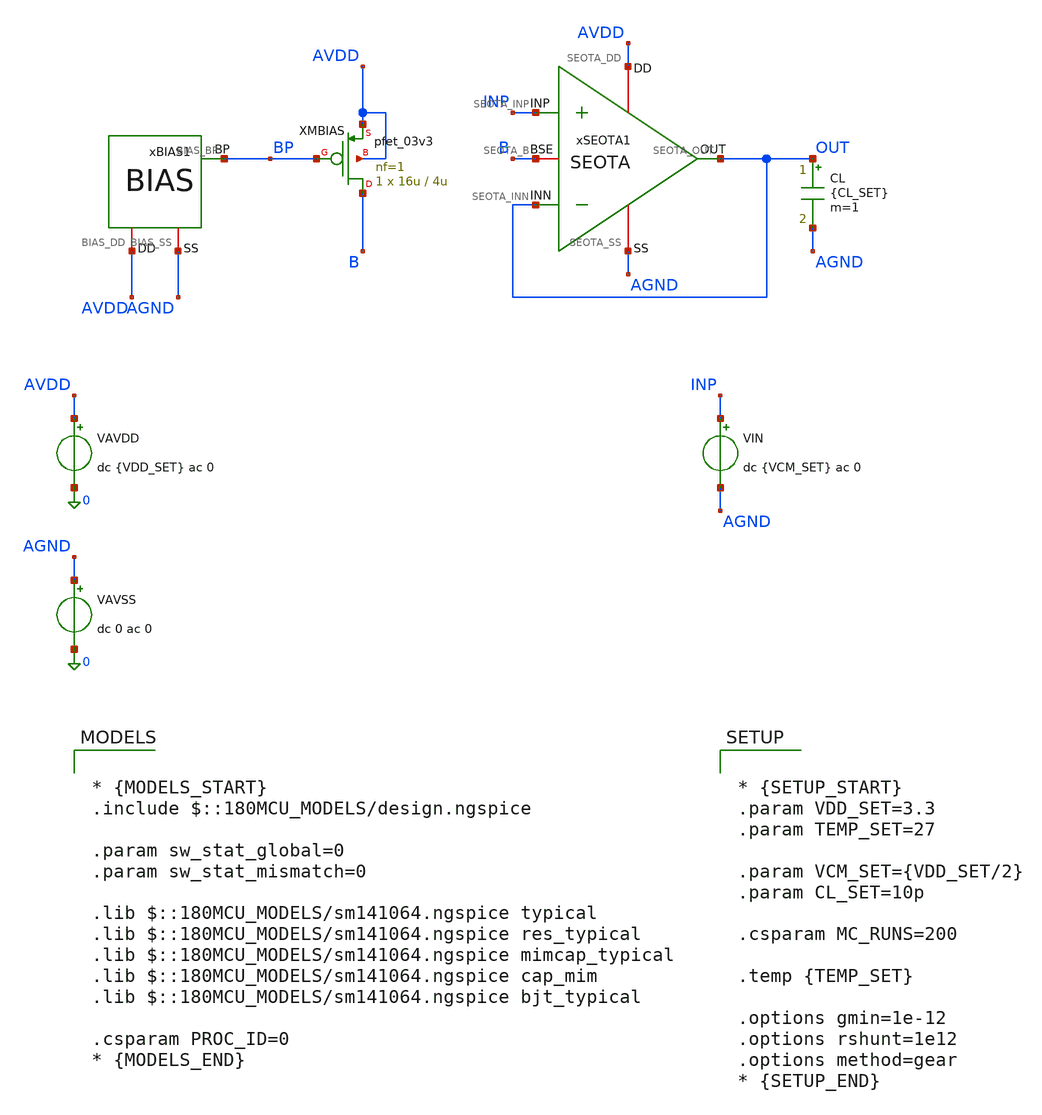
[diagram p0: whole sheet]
** sch_path: Design_Files/IC Design/Testbench/ANALOG_BLOCKS/SEOTA/Close_Loop/SEOTA_TB_CL_PVT_NOM.sch
**.subckt SEOTA_TB_CL_PVT_NOM
CL OUT AGND {CL_SET} m=1
xSEOTA1 AVDD AGND INP OUT OUT B SEOTA
VAVDD AVDD 0 dc {VDD_SET} ac 0
.save i(vavdd)
VIN INP AGND dc {VCM_SET} ac 0
VAVSS AGND 0 dc 0 ac 0
xBIAS1 AVDD AGND BP BIAS
XMBIAS B BP AVDD AVDD pfet_03v3 L=4u W=16u nf=1 ad='int((nf+1)/2) * W/nf * 0.18u' as='int((nf+2)/2) * W/nf * 0.18u'
+ pd='2*int((nf+1)/2) * (W/nf + 0.18u)' ps='2*int((nf+2)/2) * (W/nf + 0.18u)' nrd='0.18u / W' nrs='0.18u / W'
+ sa=0 sb=0 sd=0 m=1
**** begin user architecture code

* {MODELS_START}
.include $::180MCU_MODELS/design.ngspice

.param sw_stat_global=0
.param sw_stat_mismatch=0

.lib $::180MCU_MODELS/sm141064.ngspice typical
.lib $::180MCU_MODELS/sm141064.ngspice res_typical
.lib $::180MCU_MODELS/sm141064.ngspice mimcap_typical
.lib $::180MCU_MODELS/sm141064.ngspice cap_mim
.lib $::180MCU_MODELS/sm141064.ngspice bjt_typical

.csparam PROC_ID=0
* {MODELS_END}



* {SETUP_START}
.param VDD_SET=3.3
.param TEMP_SET=27

.param VCM_SET={VDD_SET/2}
.param CL_SET=10p

.csparam MC_RUNS=200

.temp {TEMP_SET}

.options gmin=1e-12
.options rshunt=1e12
.options method=gear
* {SETUP_END}




* {MEAS_START}

.control

destroy all

set noaskquit
set wr_singlescale
unset wr_vecnames

option klu
option numdgt=15
option method=gear
option maxord=2
option plotwinsize=0


if $&PROC_ID = 0
set proc=NOM
else
if $&PROC_ID = 1
set proc=FF
else
if $&PROC_ID = 2
set proc=SS
else
if $&PROC_ID = 3
set proc=FS
else
set proc=SF
end
end
end
end


shell mkdir -p /foss/designs/ECG_Acquisition_IC/Measurement_Results/IC_Simulation/ANALOG_BLOCKS/SEOTA/{$proc}.Result_txt
shell rm -f /foss/designs/ECG_Acquisition_IC/Measurement_Results/IC_Simulation/ANALOG_BLOCKS/SEOTA/{$proc}.Result_txt/{$proc}.cl_*.txt


foreach vddval 3.3 3.0 3.6
foreach tval 27 -40 125


if $vddval = 3.3

if $tval = 27
set case=nom
else
if $tval = -40
set case=tl
else
set case=th
end
end

else

if $vddval = 3.0

if $tval = 27
set case=vl
else
if $tval = -40
set case=vltl
else
set case=vlth
end
end

else

if $tval = 27
set case=vh
else
if $tval = -40
set case=vhtl
else
set case=vhth
end
end

end
end


alterparam VDD_SET=$vddval
alterparam TEMP_SET=$tval

reset

option klu

save all
save @m.xmbias.m0[id]


* OP

op

let vdd=v(AVDD)-v(AGND)
let vin=v(INP)-v(AGND)
let vout=v(OUT)-v(AGND)

let vin_diff=v(INP)-v(OUT)

let idd_total=abs(vavdd#branch)
let ibias=abs(@m.xmbias.m0[id])

wrdata /foss/designs/ECG_Acquisition_IC/Measurement_Results/IC_Simulation/ANALOG_BLOCKS/SEOTA/{$proc}.Result_txt/{$proc}.cl_{$case}_op.txt
+ vdd vin vout vin_diff v(B) idd_total ibias


* DC

dc VIN 0 $vddval 1m

let cl_vin=v(INP)-v(AGND)
let cl_vout=v(OUT)-v(AGND)

let cl_err=cl_vout-cl_vin
let cl_vin_diff=v(INP)-v(OUT)

let cl_idd=abs(vavdd#branch)
let cl_ibias=abs(@m.xmbias.m0[id])

setscale cl_vin

wrdata /foss/designs/ECG_Acquisition_IC/Measurement_Results/IC_Simulation/ANALOG_BLOCKS/SEOTA/{$proc}.Result_txt/{$proc}.cl_{$case}_dc.txt
+ cl_vout cl_err cl_vin_diff cl_idd cl_ibias


* TRAN

reset

option klu

save all
save @m.xmbias.m0[id]


if $vddval = 3.0

alter @VIN[PULSE]=[ 1.0 2.0 1u 10n 10n 10u 20u 0 ]

else

if $vddval = 3.3

alter @VIN[PULSE]=[ 1.15 2.15 1u 10n 10n 10u 20u 0 ]

else

alter @VIN[PULSE]=[ 1.3 2.3 1u 10n 10n 10u 20u 0 ]

end
end


tran 0.5n 30u

let tr_vin=v(INP)-v(AGND)
let tr_vout=v(OUT)-v(AGND)

let tr_err=tr_vout-tr_vin
let tr_vin_diff=v(INP)-v(OUT)

let tr_idd=abs(vavdd#branch)
let tr_ibias=abs(@m.xmbias.m0[id])

setscale time

wrdata /foss/designs/ECG_Acquisition_IC/Measurement_Results/IC_Simulation/ANALOG_BLOCKS/SEOTA/{$proc}.Result_txt/{$proc}.cl_{$case}_tran.txt
+ tr_vin tr_vout tr_err tr_vin_diff tr_idd tr_ibias


destroy all

end
end


quit

.endc
* {MEAS_END}


**** end user architecture code
**.ends
.end
